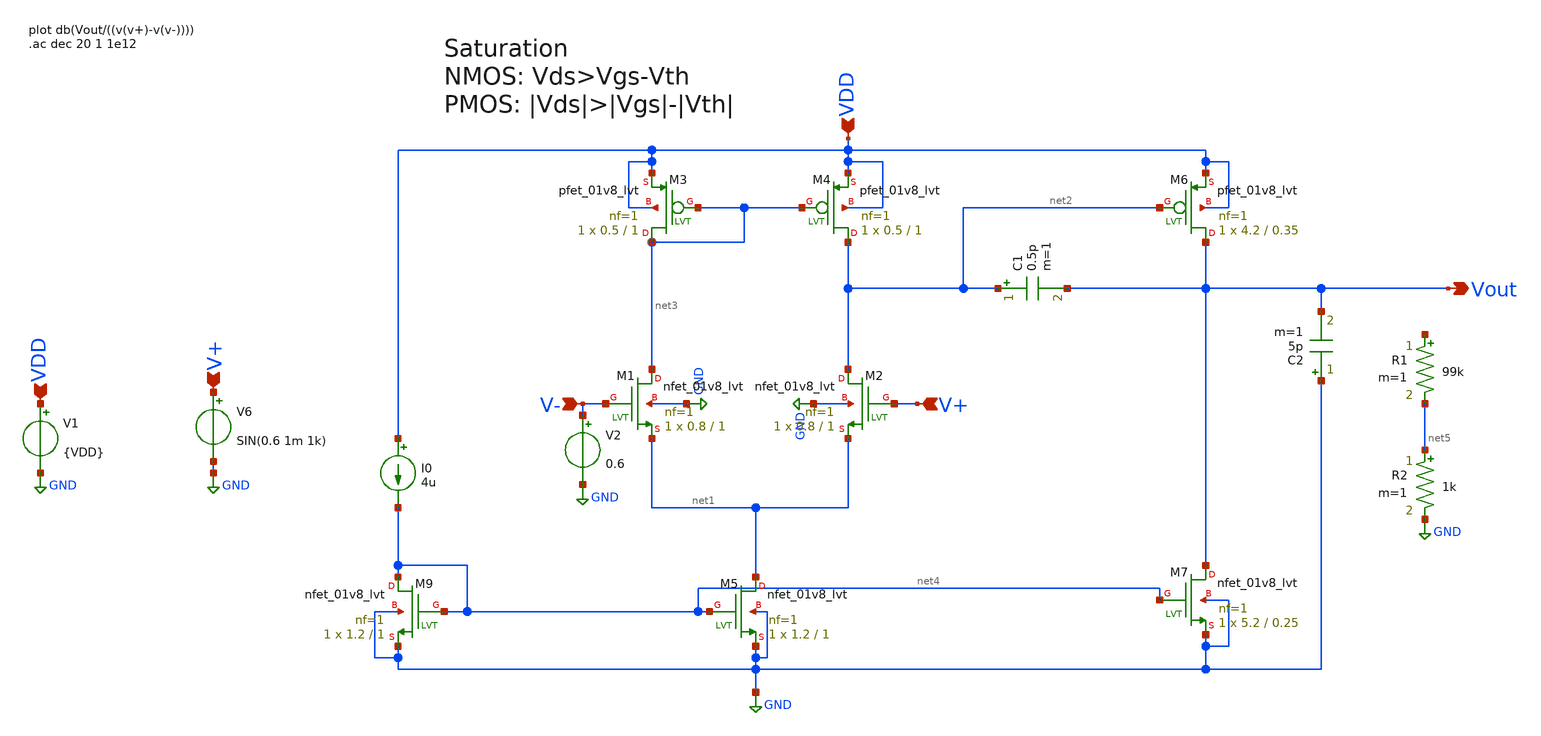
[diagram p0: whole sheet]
** sch_path: tests/headless/pdk_cases/UREx-LDO-EA_testbed.sch
**.subckt UREx-LDO-EA_testbed VDD V+ VDD Vout V+ V-
*.ipin VDD
*.ipin V+
*.ipin VDD
*.opin Vout
*.ipin V+
*.ipin V-
V1 VDD GND {VDD}
V6 V+ GND SIN(0.6 1m 1k)
C1 net2 Vout 0.5p m=1
C2 GND Vout 5p m=1
I0 VDD net4 4u
V2 V- GND 0.6
R1 net6 net5 99k m=1
R2 net5 GND 1k m=1
XM1 net3 V- net1 GND sky130_fd_pr__nfet_01v8_lvt L=1 W=0.8 nf=1 ad='int((1 + 1)/2) * 0.8 / 1 * 0.29'
+ as='int((1 + 2)/2) * 0.8 / 1 * 0.29' pd='2*int((1 + 1)/2) * (0.8 / 1 + 0.29)' ps='2*int((1 + 2)/2) * (0.8 / 1 + 0.29)'
+ nrd='0.29 / 0.8 ' nrs='0.29 / 0.8 ' sa=0 sb=0 sd=0 mult=1 m=1
XM4 net2 net3 VDD VDD sky130_fd_pr__pfet_01v8_lvt L=1 W=0.5 nf=1 ad='int((1 + 1)/2) * 0.5 / 1 * 0.29'
+ as='int((1 + 2)/2) * 0.5 / 1 * 0.29' pd='2*int((1 + 1)/2) * (0.5 / 1 + 0.29)' ps='2*int((1 + 2)/2) * (0.5 / 1 + 0.29)'
+ nrd='0.29 / 0.5 ' nrs='0.29 / 0.5 ' sa=0 sb=0 sd=0 mult=1 m=1
XM2 net2 V+ net1 GND sky130_fd_pr__nfet_01v8_lvt L=1 W=0.8 nf=1 ad='int((1 + 1)/2) * 0.8 / 1 * 0.29'
+ as='int((1 + 2)/2) * 0.8 / 1 * 0.29' pd='2*int((1 + 1)/2) * (0.8 / 1 + 0.29)' ps='2*int((1 + 2)/2) * (0.8 / 1 + 0.29)'
+ nrd='0.29 / 0.8 ' nrs='0.29 / 0.8 ' sa=0 sb=0 sd=0 mult=1 m=1
XM9 net4 net4 GND GND sky130_fd_pr__nfet_01v8_lvt L=1 W=1.2 nf=1 ad='int((1 + 1)/2) * 1.2 / 1 * 0.29'
+ as='int((1 + 2)/2) * 1.2 / 1 * 0.29' pd='2*int((1 + 1)/2) * (1.2 / 1 + 0.29)' ps='2*int((1 + 2)/2) * (1.2 / 1 + 0.29)'
+ nrd='0.29 / 1.2 ' nrs='0.29 / 1.2 ' sa=0 sb=0 sd=0 mult=1 m=1
XM5 net1 net4 GND GND sky130_fd_pr__nfet_01v8_lvt L=1 W=1.2 nf=1 ad='int((1 + 1)/2) * 1.2 / 1 * 0.29'
+ as='int((1 + 2)/2) * 1.2 / 1 * 0.29' pd='2*int((1 + 1)/2) * (1.2 / 1 + 0.29)' ps='2*int((1 + 2)/2) * (1.2 / 1 + 0.29)'
+ nrd='0.29 / 1.2 ' nrs='0.29 / 1.2 ' sa=0 sb=0 sd=0 mult=1 m=1
XM7 Vout net4 GND GND sky130_fd_pr__nfet_01v8_lvt L=0.25 W=5.2 nf=1 ad='int((1 + 1)/2) * 5.2 / 1 * 0.29'
+ as='int((1 + 2)/2) * 5.2 / 1 * 0.29' pd='2*int((1 + 1)/2) * (5.2 / 1 + 0.29)' ps='2*int((1 + 2)/2) * (5.2 / 1 + 0.29)'
+ nrd='0.29 / 5.2 ' nrs='0.29 / 5.2 ' sa=0 sb=0 sd=0 mult=1 m=1
XM3 net3 net3 VDD VDD sky130_fd_pr__pfet_01v8_lvt L=1 W=0.5 nf=1 ad='int((1 + 1)/2) * 0.5 / 1 * 0.29'
+ as='int((1 + 2)/2) * 0.5 / 1 * 0.29' pd='2*int((1 + 1)/2) * (0.5 / 1 + 0.29)' ps='2*int((1 + 2)/2) * (0.5 / 1 + 0.29)'
+ nrd='0.29 / 0.5 ' nrs='0.29 / 0.5 ' sa=0 sb=0 sd=0 mult=1 m=1
XM6 Vout net2 VDD VDD sky130_fd_pr__pfet_01v8_lvt L=0.35 W=4.2 nf=1 ad='int((1 + 1)/2) * 4.2 / 1 * 0.29'
+ as='int((1 + 2)/2) * 4.2 / 1 * 0.29' pd='2*int((1 + 1)/2) * (4.2 / 1 + 0.29)' ps='2*int((1 + 2)/2) * (4.2 / 1 + 0.29)'
+ nrd='0.29 / 4.2 ' nrs='0.29 / 4.2 ' sa=0 sb=0 sd=0 mult=1 m=1
**** begin user architecture code



.lib /usr/local/share/pdk/sky130A/libs.tech/ngspice/sky130.lib.spice tt
.param VDD=1.8 amp=1.2
.tran 5u 5m
*.ac dec 20 1 1e12
.save all

.control
run
*plot -i(v1)
plot vout
*plot db(vout/v(v+))
*plot 180*cph(vout)/pi
set wr_singlescale
set wr_vecnames
*wrdata /foss/designs/2stageCMOSOpAmp/sim_data/GainvsFreq/gain(max).txt db(vout/v(v+))
*wrdata /foss/designs/2stageCMOSOpAmp/sim_data/sample_waves/a1.3m_f1k_gain700.txt vout
*wrdata /foss/designs/2stageCMOSOpAmp/sim_data/SR/SR.txt vout

.endc


**** end user architecture code
**.ends
.GLOBAL GND
.end
